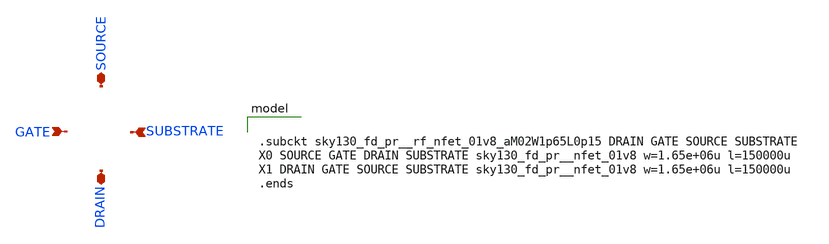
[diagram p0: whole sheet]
** sch_path: xschem/sky130_fd_pr__rf_nfet_01v8_aM02W1p65L0p15.sch
**.subckt sky130_fd_pr__rf_nfet_01v8_aM02W1p65L0p15 SOURCE DRAIN SUBSTRATE GATE
*.iopin SOURCE
*.iopin DRAIN
*.ipin SUBSTRATE
*.ipin GATE
**** begin user architecture code


.subckt sky130_fd_pr__rf_nfet_01v8_aM02W1p65L0p15 DRAIN GATE SOURCE SUBSTRATE
X0 SOURCE GATE DRAIN SUBSTRATE sky130_fd_pr__nfet_01v8 w=1.65e+06u l=150000u
X1 DRAIN GATE SOURCE SUBSTRATE sky130_fd_pr__nfet_01v8 w=1.65e+06u l=150000u
.ends

**** end user architecture code
**.ends
.end
